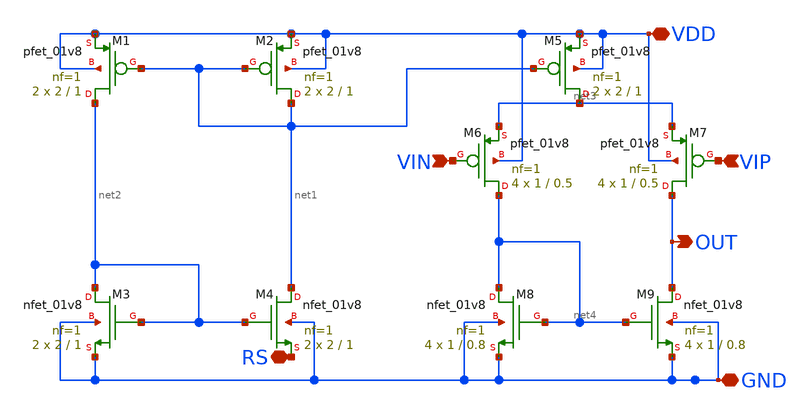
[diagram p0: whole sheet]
** sch_path: opamp1stage/xschem/opamp1s.sch
**.subckt opamp1s VIN VIP RS GND VDD OUT
*.ipin VIN
*.ipin VIP
*.iopin RS
*.iopin GND
*.iopin VDD
*.opin OUT
XM3 net2 net2 GND GND sky130_fd_pr__nfet_01v8 L=1 W=2 nf=1 ad='int((nf+1)/2) * W/nf * 0.29' as='int((nf+2)/2) * W/nf * 0.29'
+ pd='2*int((nf+1)/2) * (W/nf + 0.29)' ps='2*int((nf+2)/2) * (W/nf + 0.29)' nrd='0.29 / W' nrs='0.29 / W'
+ sa=0 sb=0 sd=0 mult=2 m=2
XM1 net2 net1 VDD VDD sky130_fd_pr__pfet_01v8 L=1 W=2 nf=1 ad='int((nf+1)/2) * W/nf * 0.29' as='int((nf+2)/2) * W/nf * 0.29'
+ pd='2*int((nf+1)/2) * (W/nf + 0.29)' ps='2*int((nf+2)/2) * (W/nf + 0.29)' nrd='0.29 / W' nrs='0.29 / W'
+ sa=0 sb=0 sd=0 mult=2 m=2
XM2 net1 net1 VDD VDD sky130_fd_pr__pfet_01v8 L=1 W=2 nf=1 ad='int((nf+1)/2) * W/nf * 0.29' as='int((nf+2)/2) * W/nf * 0.29'
+ pd='2*int((nf+1)/2) * (W/nf + 0.29)' ps='2*int((nf+2)/2) * (W/nf + 0.29)' nrd='0.29 / W' nrs='0.29 / W'
+ sa=0 sb=0 sd=0 mult=2 m=2
XM4 net1 net2 RS GND sky130_fd_pr__nfet_01v8 L=1 W=2 nf=1 ad='int((nf+1)/2) * W/nf * 0.29' as='int((nf+2)/2) * W/nf * 0.29'
+ pd='2*int((nf+1)/2) * (W/nf + 0.29)' ps='2*int((nf+2)/2) * (W/nf + 0.29)' nrd='0.29 / W' nrs='0.29 / W'
+ sa=0 sb=0 sd=0 mult=2 m=2
XM5 net3 net1 VDD VDD sky130_fd_pr__pfet_01v8 L=1 W=2 nf=1 ad='int((nf+1)/2) * W/nf * 0.29' as='int((nf+2)/2) * W/nf * 0.29'
+ pd='2*int((nf+1)/2) * (W/nf + 0.29)' ps='2*int((nf+2)/2) * (W/nf + 0.29)' nrd='0.29 / W' nrs='0.29 / W'
+ sa=0 sb=0 sd=0 mult=2 m=2
XM6 net4 VIN net3 VDD sky130_fd_pr__pfet_01v8 L=0.5 W=1 nf=1 ad='int((nf+1)/2) * W/nf * 0.29' as='int((nf+2)/2) * W/nf * 0.29'
+ pd='2*int((nf+1)/2) * (W/nf + 0.29)' ps='2*int((nf+2)/2) * (W/nf + 0.29)' nrd='0.29 / W' nrs='0.29 / W'
+ sa=0 sb=0 sd=0 mult=4 m=4
XM7 OUT VIP net3 VDD sky130_fd_pr__pfet_01v8 L=0.5 W=1 nf=1 ad='int((nf+1)/2) * W/nf * 0.29' as='int((nf+2)/2) * W/nf * 0.29'
+ pd='2*int((nf+1)/2) * (W/nf + 0.29)' ps='2*int((nf+2)/2) * (W/nf + 0.29)' nrd='0.29 / W' nrs='0.29 / W'
+ sa=0 sb=0 sd=0 mult=4 m=4
XM8 net4 net4 GND GND sky130_fd_pr__nfet_01v8 L=0.8 W=1 nf=1 ad='int((nf+1)/2) * W/nf * 0.29' as='int((nf+2)/2) * W/nf * 0.29'
+ pd='2*int((nf+1)/2) * (W/nf + 0.29)' ps='2*int((nf+2)/2) * (W/nf + 0.29)' nrd='0.29 / W' nrs='0.29 / W'
+ sa=0 sb=0 sd=0 mult=4 m=4
XM9 OUT net4 GND GND sky130_fd_pr__nfet_01v8 L=0.8 W=1 nf=1 ad='int((nf+1)/2) * W/nf * 0.29' as='int((nf+2)/2) * W/nf * 0.29'
+ pd='2*int((nf+1)/2) * (W/nf + 0.29)' ps='2*int((nf+2)/2) * (W/nf + 0.29)' nrd='0.29 / W' nrs='0.29 / W'
+ sa=0 sb=0 sd=0 mult=4 m=4
**.ends
.end
